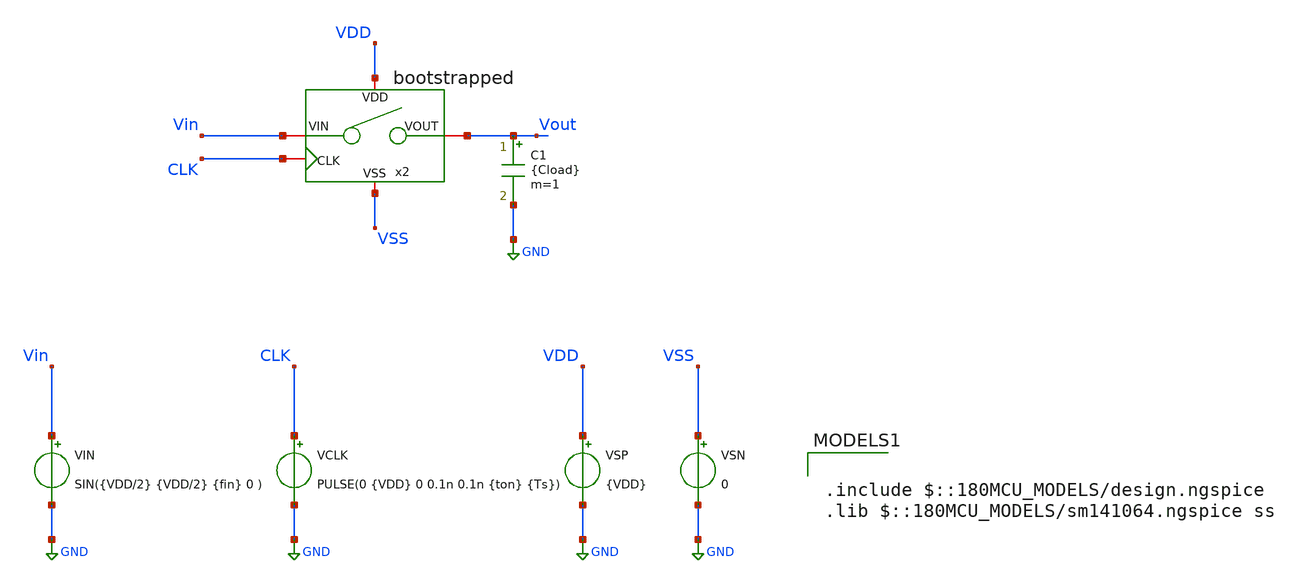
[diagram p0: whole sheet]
** sch_path: designs/sar_adc/samplehold/bootstrapped/xschem/tb_bootstrapped.sch
**.subckt tb_bootstrapped
VSP VDD GND {VDD}
VSN VSS GND 0
VIN Vin GND SIN({VDD/2} {VDD/2} {fin} 0 )
VCLK CLK GND PULSE(0 {VDD} 0 0.1n 0.1n {ton} {Ts})
C1 Vout GND {Cload} m=1
x2 VDD VSS CLK Vin Vout bootstrapped
**** begin user architecture code

.include $::180MCU_MODELS/design.ngspice
.lib $::180MCU_MODELS/sm141064.ngspice ss




* Input parameters
.param Fs = 5Meg
.param Ns = 1024
.param Nc = 509
.param fin = Nc/Ns*Fs

* Sampling clock
.param Ts = 1/Fs
.param ton = Ts/12

* Test-bench parameters
.temp 27
.param VDD = 3.3
.param Cload = 1p

.save all

.control

* Local variables for .control
let Fs = 5Meg
let Ns = 1024
let Nspare = 5

let tstep = 1/(Fs*240)
let tstop = (Ns + Nspare)/Fs

* Transient simulation
tran $&tstep $&tstop

linearize v(vout) v(vin) v(clk)
wrdata tb_bootstrapped.csv v(vin) v(vout) v(clk)

plot v(vin) v(vout)
plot v(vin) v(vout) xl 0 4u

.endc



**** end user architecture code
**.ends
.GLOBAL GND
.end
